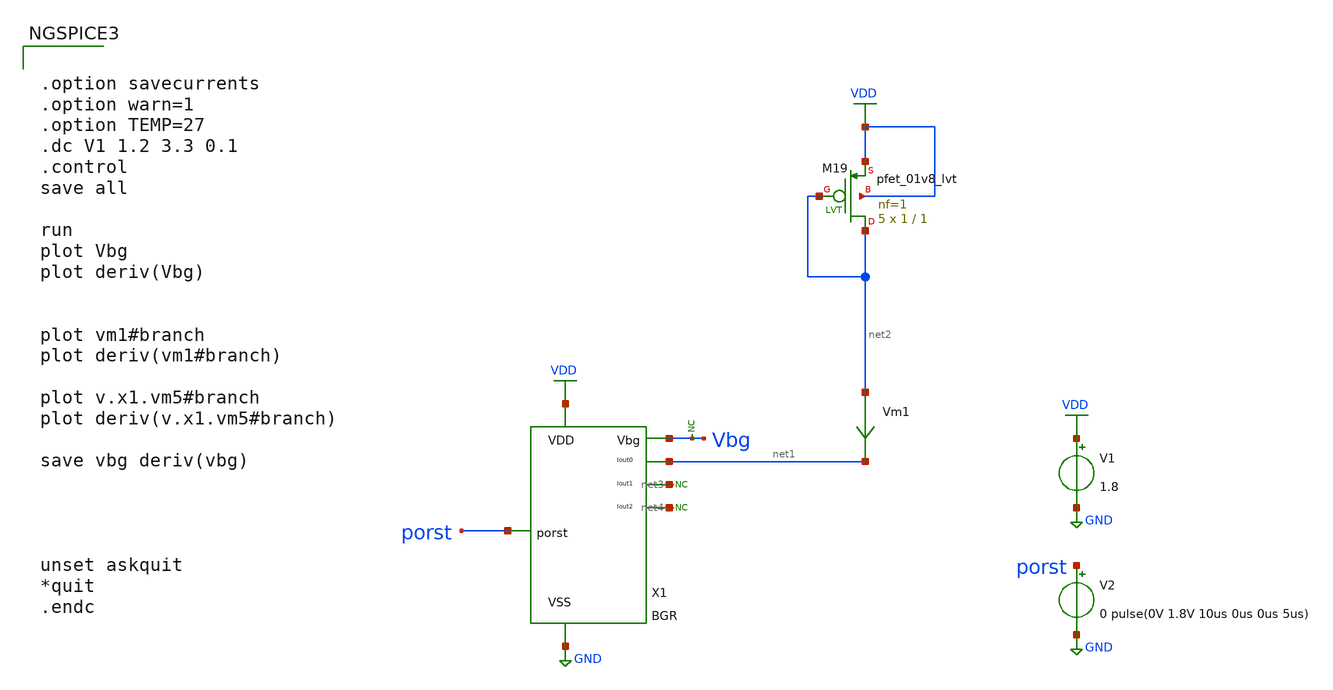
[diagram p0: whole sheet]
** sch_path: design/bgr_new/tb_BGR_vc.sch
**.subckt tb_BGR_vc
V1 VDD GND 1.8
V2 porst GND 0 pulse(0V 1.8V 10us 0us 0us 5us)
* noconn #net3
* noconn #net4
XM19 net2 net2 VDD VDD sky130_fd_pr__pfet_01v8_lvt L=1 W=1 nf=1 ad='int((nf+1)/2) * W/nf * 0.29' as='int((nf+2)/2) * W/nf * 0.29'
+ pd='2*int((nf+1)/2) * (W/nf + 0.29)' ps='2*int((nf+2)/2) * (W/nf + 0.29)' nrd='0.29 / W' nrs='0.29 / W'
+ sa=0 sb=0 sd=0 mult=5 m=5
Vm1 net2 net1 0
.save i(vm1)
* noconn Vbg
X1 porst VDD GND Vbg net1 net3 net4 BGR
**** begin user architecture code

** opencircuitdesign pdks install
.lib $::SKYWATER_MODELS/sky130.lib.spice tt




.option savecurrents
.option warn=1
.option TEMP=27
.dc V1 1.2 3.3 0.1
.control
save all

run
plot Vbg
plot deriv(Vbg)


plot vm1#branch
plot deriv(vm1#branch)

plot v.x1.vm5#branch
plot deriv(v.x1.vm5#branch)

save vbg deriv(vbg)




unset askquit
*quit
.endc


**** end user architecture code
**.ends
.GLOBAL VDD
.GLOBAL GND
.end
